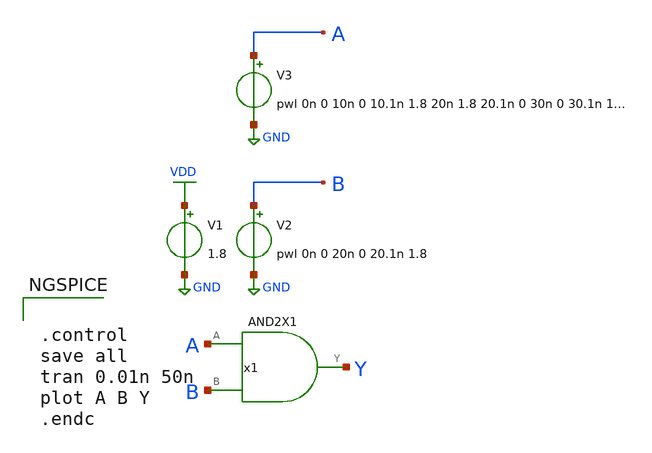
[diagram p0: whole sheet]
** sch_path: lib/xschem/test_AND2X1.sch
**.subckt test_AND2X1
V2 B GND pwl 0n 0 20n 0 20.1n 1.8
V1 VDD GND 1.8
V3 A GND pwl 0n 0 10n 0 10.1n 1.8 20n 1.8 20.1n 0 30n 0 30.1n 1.8 40n 1.8 40.1n 0
x1 Y A B VDD GND AND2X1
**** begin user architecture code

.lib $::SKYWATER_MODELS/sky130.lib.spice tt


**** end user architecture code
**.ends

* expanding   symbol:  AND2X1.sym # of pins=3
** sym_path: lib/xschem/AND2X1.sym
** sch_path: lib/xschem/AND2X1.sch
.subckt AND2X1 Y A B VCCPIN VSSPIN
*.ipin A
*.ipin B
*.opin Y
x1 net1 A B VCCPIN VSSPIN NAND2X1
x2 Y net1 VCCPIN VSSPIN INVX1
.ends


* expanding   symbol:  NAND2X1.sym # of pins=3
** sym_path: lib/xschem/NAND2X1.sym
** sch_path: lib/xschem/NAND2X1.sch
.subckt NAND2X1 Y A B VCCPIN VSSPIN
*.ipin A
*.opin Y
*.ipin B
XM1 Y A VCCPIN VCCPIN sky130_fd_pr__pfet_01v8 L=0.15 W=2 nf=1 ad='int((nf+1)/2) * W/nf * 0.29' as='int((nf+2)/2) * W/nf * 0.29'
+ pd='2*int((nf+1)/2) * (W/nf + 0.29)' ps='2*int((nf+2)/2) * (W/nf + 0.29)' nrd='0.29 / W' nrs='0.29 / W'
+ sa=0 sb=0 sd=0 mult=1 m=1
XM5 Y A net1 VSSPIN sky130_fd_pr__nfet_01v8 L=0.15 W=3 nf=1 ad='int((nf+1)/2) * W/nf * 0.29' as='int((nf+2)/2) * W/nf * 0.29'
+ pd='2*int((nf+1)/2) * (W/nf + 0.29)' ps='2*int((nf+2)/2) * (W/nf + 0.29)' nrd='0.29 / W' nrs='0.29 / W'
+ sa=0 sb=0 sd=0 mult=1 m=1
XM2 Y A VCCPIN VCCPIN sky130_fd_pr__pfet_01v8 L=0.15 W=2 nf=1 ad='int((nf+1)/2) * W/nf * 0.29' as='int((nf+2)/2) * W/nf * 0.29'
+ pd='2*int((nf+1)/2) * (W/nf + 0.29)' ps='2*int((nf+2)/2) * (W/nf + 0.29)' nrd='0.29 / W' nrs='0.29 / W'
+ sa=0 sb=0 sd=0 mult=1 m=1
XM3 Y B VCCPIN VCCPIN sky130_fd_pr__pfet_01v8 L=0.15 W=2 nf=1 ad='int((nf+1)/2) * W/nf * 0.29' as='int((nf+2)/2) * W/nf * 0.29'
+ pd='2*int((nf+1)/2) * (W/nf + 0.29)' ps='2*int((nf+2)/2) * (W/nf + 0.29)' nrd='0.29 / W' nrs='0.29 / W'
+ sa=0 sb=0 sd=0 mult=1 m=1
XM4 Y B VCCPIN VCCPIN sky130_fd_pr__pfet_01v8 L=0.15 W=2 nf=1 ad='int((nf+1)/2) * W/nf * 0.29' as='int((nf+2)/2) * W/nf * 0.29'
+ pd='2*int((nf+1)/2) * (W/nf + 0.29)' ps='2*int((nf+2)/2) * (W/nf + 0.29)' nrd='0.29 / W' nrs='0.29 / W'
+ sa=0 sb=0 sd=0 mult=1 m=1
XM6 net1 B VSSPIN VSSPIN sky130_fd_pr__nfet_01v8 L=0.15 W=3 nf=1 ad='int((nf+1)/2) * W/nf * 0.29' as='int((nf+2)/2) * W/nf * 0.29'
+ pd='2*int((nf+1)/2) * (W/nf + 0.29)' ps='2*int((nf+2)/2) * (W/nf + 0.29)' nrd='0.29 / W' nrs='0.29 / W'
+ sa=0 sb=0 sd=0 mult=1 m=1
.ends


* expanding   symbol:  INVX1.sym # of pins=2
** sym_path: lib/xschem/INVX1.sym
** sch_path: lib/xschem/INVX1.sch
.subckt INVX1 Y A VCCPIN VSSPIN
*.ipin A
*.opin Y
XM1 Y A VSSPIN VSSPIN sky130_fd_pr__nfet_01v8 L=0.15 W=3 nf=1 ad='int((nf+1)/2) * W/nf * 0.29' as='int((nf+2)/2) * W/nf * 0.29'
+ pd='2*int((nf+1)/2) * (W/nf + 0.29)' ps='2*int((nf+2)/2) * (W/nf + 0.29)' nrd='0.29 / W' nrs='0.29 / W'
+ sa=0 sb=0 sd=0 mult=1 m=1
XM2 Y A VCCPIN VCCPIN sky130_fd_pr__pfet_01v8 L=0.15 W=2 nf=1 ad='int((nf+1)/2) * W/nf * 0.29' as='int((nf+2)/2) * W/nf * 0.29'
+ pd='2*int((nf+1)/2) * (W/nf + 0.29)' ps='2*int((nf+2)/2) * (W/nf + 0.29)' nrd='0.29 / W' nrs='0.29 / W'
+ sa=0 sb=0 sd=0 mult=1 m=1
XM3 Y A VCCPIN VCCPIN sky130_fd_pr__pfet_01v8 L=0.15 W=2 nf=1 ad='int((nf+1)/2) * W/nf * 0.29' as='int((nf+2)/2) * W/nf * 0.29'
+ pd='2*int((nf+1)/2) * (W/nf + 0.29)' ps='2*int((nf+2)/2) * (W/nf + 0.29)' nrd='0.29 / W' nrs='0.29 / W'
+ sa=0 sb=0 sd=0 mult=1 m=1
.ends

.GLOBAL VDD
.GLOBAL GND
**** begin user architecture code


.control
save all
tran 0.01n 50n
plot A B Y
.endc


**** end user architecture code
.end
